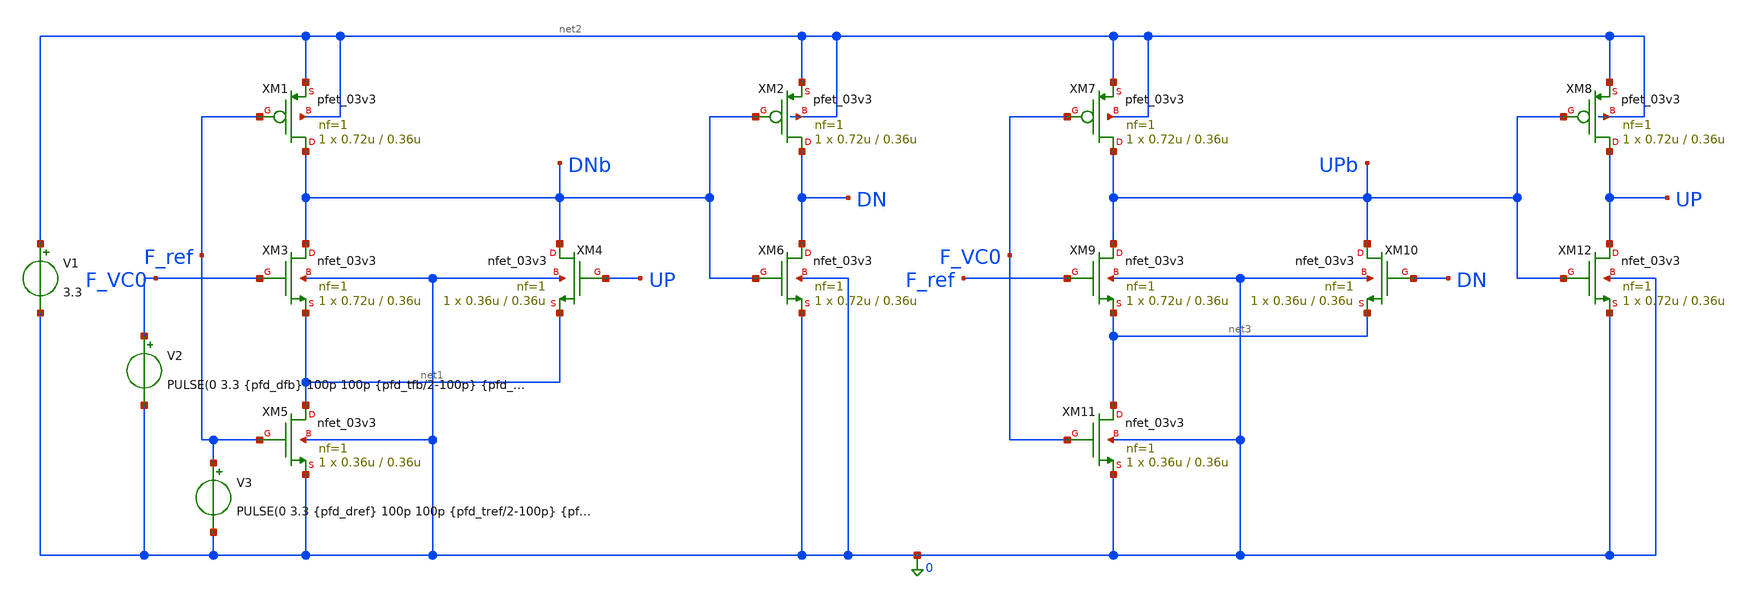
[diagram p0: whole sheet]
** sch_path: PLL/analog/schematics/Phase_Detector_FE.sch
**.subckt Phase_Detector_FE
XM1 DNb F_ref net2 net2 pfet_03v3 L=0.36u W=0.72u nf=1 ad='int((nf+1)/2) * W/nf * 0.18u' as='int((nf+2)/2) * W/nf * 0.18u'
+ pd='2*int((nf+1)/2) * (W/nf + 0.18u)' ps='2*int((nf+2)/2) * (W/nf + 0.18u)' nrd='0.18u / W' nrs='0.18u / W'
+ sa=0 sb=0 sd=0 m=1
XM2 DN DNb net2 net2 pfet_03v3 L=0.36u W=0.72u nf=1 ad='int((nf+1)/2) * W/nf * 0.18u' as='int((nf+2)/2) * W/nf * 0.18u'
+ pd='2*int((nf+1)/2) * (W/nf + 0.18u)' ps='2*int((nf+2)/2) * (W/nf + 0.18u)' nrd='0.18u / W' nrs='0.18u / W'
+ sa=0 sb=0 sd=0 m=1
XM3 DNb F_VC0 net1 0 nfet_03v3 L=0.36u W=0.72u nf=1 ad='int((nf+1)/2) * W/nf * 0.18u' as='int((nf+2)/2) * W/nf * 0.18u'
+ pd='2*int((nf+1)/2) * (W/nf + 0.18u)' ps='2*int((nf+2)/2) * (W/nf + 0.18u)' nrd='0.18u / W' nrs='0.18u / W'
+ sa=0 sb=0 sd=0 m=1
XM4 DNb UP net1 0 nfet_03v3 L=0.36u W=0.36u nf=1 ad='int((nf+1)/2) * W/nf * 0.18u' as='int((nf+2)/2) * W/nf * 0.18u'
+ pd='2*int((nf+1)/2) * (W/nf + 0.18u)' ps='2*int((nf+2)/2) * (W/nf + 0.18u)' nrd='0.18u / W' nrs='0.18u / W'
+ sa=0 sb=0 sd=0 m=1
XM5 net1 F_ref 0 0 nfet_03v3 L=0.36u W=0.36u nf=1 ad='int((nf+1)/2) * W/nf * 0.18u' as='int((nf+2)/2) * W/nf * 0.18u'
+ pd='2*int((nf+1)/2) * (W/nf + 0.18u)' ps='2*int((nf+2)/2) * (W/nf + 0.18u)' nrd='0.18u / W' nrs='0.18u / W'
+ sa=0 sb=0 sd=0 m=1
XM6 DN DNb 0 0 nfet_03v3 L=0.36u W=0.72u nf=1 ad='int((nf+1)/2) * W/nf * 0.18u' as='int((nf+2)/2) * W/nf * 0.18u'
+ pd='2*int((nf+1)/2) * (W/nf + 0.18u)' ps='2*int((nf+2)/2) * (W/nf + 0.18u)' nrd='0.18u / W' nrs='0.18u / W'
+ sa=0 sb=0 sd=0 m=1
XM7 UPb F_VC0 net2 net2 pfet_03v3 L=0.36u W=0.72u nf=1 ad='int((nf+1)/2) * W/nf * 0.18u' as='int((nf+2)/2) * W/nf * 0.18u'
+ pd='2*int((nf+1)/2) * (W/nf + 0.18u)' ps='2*int((nf+2)/2) * (W/nf + 0.18u)' nrd='0.18u / W' nrs='0.18u / W'
+ sa=0 sb=0 sd=0 m=1
XM8 UP UPb net2 net2 pfet_03v3 L=0.36u W=0.72u nf=1 ad='int((nf+1)/2) * W/nf * 0.18u' as='int((nf+2)/2) * W/nf * 0.18u'
+ pd='2*int((nf+1)/2) * (W/nf + 0.18u)' ps='2*int((nf+2)/2) * (W/nf + 0.18u)' nrd='0.18u / W' nrs='0.18u / W'
+ sa=0 sb=0 sd=0 m=1
XM9 UPb F_ref net3 0 nfet_03v3 L=0.36u W=0.72u nf=1 ad='int((nf+1)/2) * W/nf * 0.18u' as='int((nf+2)/2) * W/nf * 0.18u'
+ pd='2*int((nf+1)/2) * (W/nf + 0.18u)' ps='2*int((nf+2)/2) * (W/nf + 0.18u)' nrd='0.18u / W' nrs='0.18u / W'
+ sa=0 sb=0 sd=0 m=1
XM10 UPb DN net3 0 nfet_03v3 L=0.36u W=0.36u nf=1 ad='int((nf+1)/2) * W/nf * 0.18u' as='int((nf+2)/2) * W/nf * 0.18u'
+ pd='2*int((nf+1)/2) * (W/nf + 0.18u)' ps='2*int((nf+2)/2) * (W/nf + 0.18u)' nrd='0.18u / W' nrs='0.18u / W'
+ sa=0 sb=0 sd=0 m=1
XM11 net3 F_VC0 0 0 nfet_03v3 L=0.36u W=0.36u nf=1 ad='int((nf+1)/2) * W/nf * 0.18u' as='int((nf+2)/2) * W/nf * 0.18u'
+ pd='2*int((nf+1)/2) * (W/nf + 0.18u)' ps='2*int((nf+2)/2) * (W/nf + 0.18u)' nrd='0.18u / W' nrs='0.18u / W'
+ sa=0 sb=0 sd=0 m=1
XM12 UP UPb 0 0 nfet_03v3 L=0.36u W=0.72u nf=1 ad='int((nf+1)/2) * W/nf * 0.18u' as='int((nf+2)/2) * W/nf * 0.18u'
+ pd='2*int((nf+1)/2) * (W/nf + 0.18u)' ps='2*int((nf+2)/2) * (W/nf + 0.18u)' nrd='0.18u / W' nrs='0.18u / W'
+ sa=0 sb=0 sd=0 m=1
V1 net2 0 3.3
V2 F_VC0 0 PULSE(0 3.3 {pfd_dfb} 100p 100p {pfd_tfb/2-100p} {pfd_tfb})
V3 F_ref 0 PULSE(0 3.3 {pfd_dref} 100p 100p {pfd_tref/2-100p} {pfd_tref})
**** begin user architecture code



.include /foss/pdks/gf180mcuD/libs.tech/ngspice/design.ngspice
.lib /foss/pdks/gf180mcuD/libs.tech/ngspice/sm141064.ngspice typical

.temp 27

* Nominal frequency: 40 MHz
.param pfd_tref=25n pfd_tfb=25n
.param pfd_dref=10n pfd_dfb=10n

* Input clocks: 3.3 V, 100 ps edges, 50% duty cycle

.control
set noaskquit
set numdgt=7

foreach test 1 2 3 4 5

  * Restore nominal settings before selecting each case
  alterparam pfd_tfb=25n
  alterparam pfd_dref=10n
  alterparam pfd_dfb=10n

  if $test = 1
    alterparam pfd_dfb=12n
    echo CASE_1_REF_LEADS_BY_2ns
  end

  if $test = 2
    alterparam pfd_dref=12n
    echo CASE_2_FEEDBACK_LEADS_BY_2ns
  end

  if $test = 3
    echo CASE_3_ALIGNED_CLOCKS
  end

  if $test = 4
    alterparam pfd_tfb=25.641025641n
    echo CASE_4_FEEDBACK_39MHz
  end

  if $test = 5
    alterparam pfd_tfb=24.390243902n
    echo CASE_5_FEEDBACK_41MHz
  end

  reset
  save v(F_ref) v(F_VC0) v(UP) v(DN) v(UPb) v(DNb)

  * Run 2.5 us; maximum timestep 10 ps
  tran 10p 2.5u 0 10p

  * Convert outputs to logic levels using a 1.65 V threshold
  let up_logic = (v(UP) gt 1.65)
  let dn_logic = (v(DN) gt 1.65)
  let both_on = up_logic * dn_logic

  * Ignore the first 500 ns
  meas tran up_duty AVG up_logic FROM=500n TO=2.5u
  meas tran dn_duty AVG dn_logic FROM=500n TO=2.5u
  meas tran overlap_duty AVG both_on FROM=500n TO=2.5u

  * Positive means UP dominates; negative means DN dominates
  let duty_error = up_duty - dn_duty
  print duty_error

  * Vertical offsets separate the displayed waveforms
  let ref_trace = v(F_ref) + 12
  let fb_trace = v(F_VC0) + 8
  let up_trace = v(UP) + 4

  if $test < 4
    plot ref_trace fb_trace up_trace v(DN) xlimit 500n 600n title PFD_case_{$test}
  else
    plot ref_trace fb_trace up_trace v(DN) xlimit 500n 1.5u title PFD_case_{$test}
  end

end
.endc



**** end user architecture code
**.ends
.end
